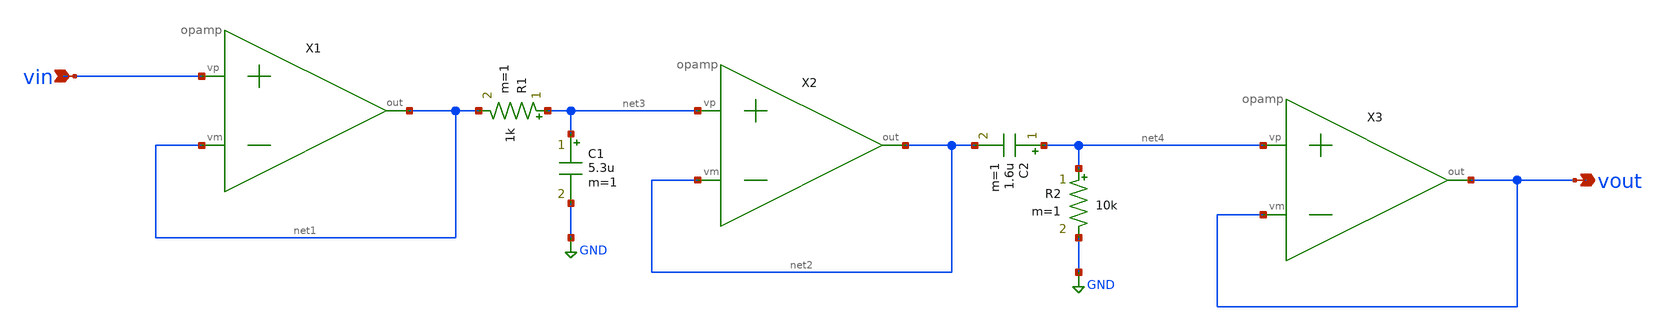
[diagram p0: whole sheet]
** sch_path: xschem/FILTER/ideal_FILTER.sch
**.subckt ideal_FILTER vin vout
*.ipin vin
*.opin vout
X1 vin net1 net1 opamp
X2 net3 net2 net2 opamp
X3 net4 vout vout opamp
R1 net3 net1 1k m=1
R2 net4 GND 10k m=1
C1 net3 GND 5.3u m=1
C2 net4 net2 1.6u m=1
**.ends

* expanding   symbol:  MISC/opamp.sym # of pins=3
** sym_path: xschem/MISC/opamp.sym
** sch_path: xschem/MISC/opamp.sch
.subckt opamp vp vm out
*.ipin vp
*.ipin vm
*.opin out
E1 out GND vp vm 1E6
.ends

.GLOBAL GND
.end
